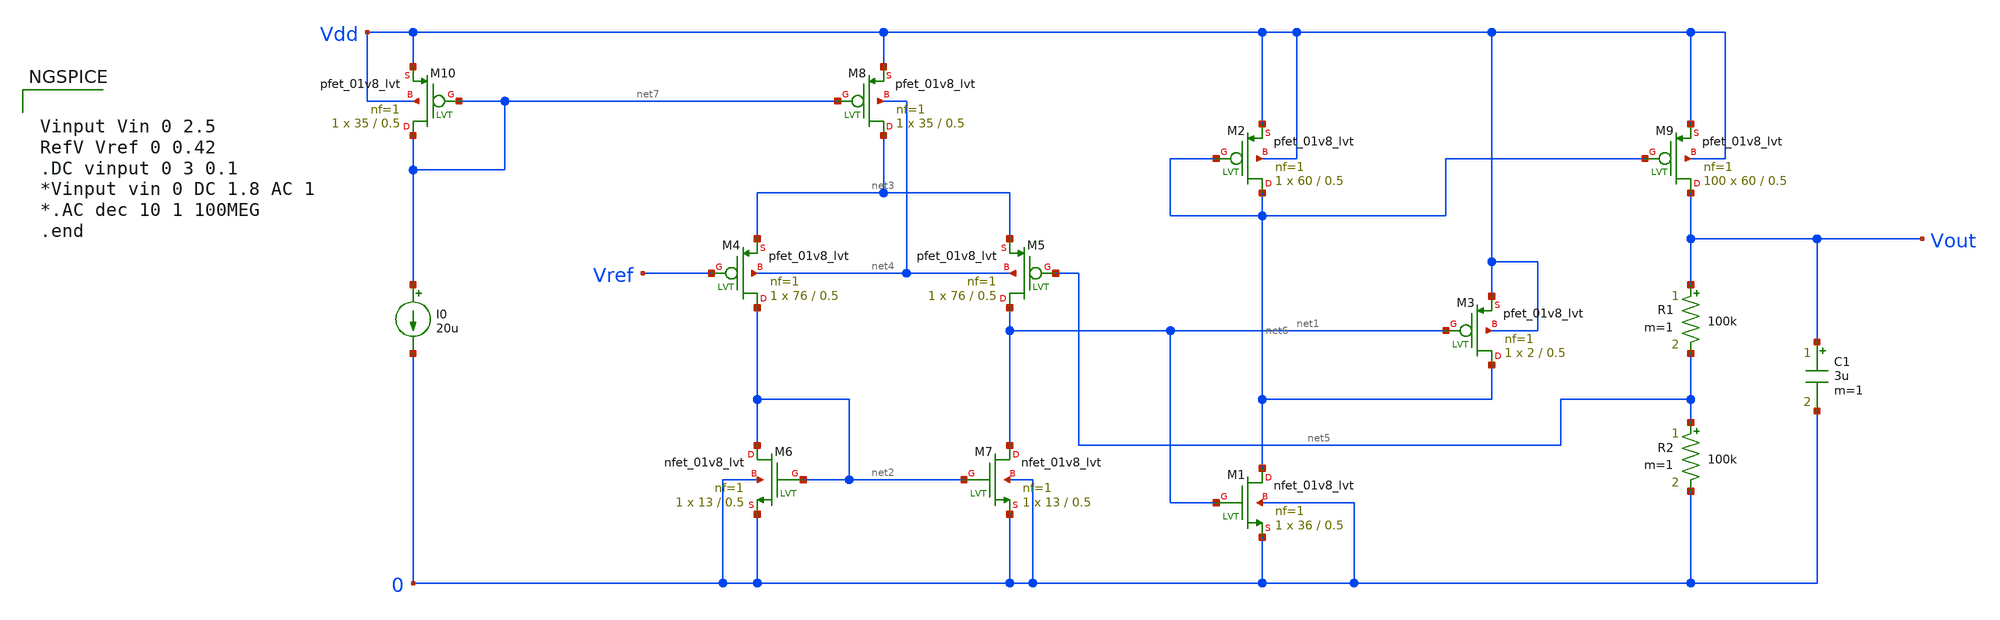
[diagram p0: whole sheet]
** sch_path: LDO/Schematic/Low_PSR_LDO.sch
**.subckt Low_PSR_LDO
XM1 net6 net1 0 0 sky130_fd_pr__nfet_01v8_lvt L=0.5 W=36 nf=1 ad='int((nf+1)/2) * W/nf * 0.29' as='int((nf+2)/2) * W/nf * 0.29'
+ pd='2*int((nf+1)/2) * (W/nf + 0.29)' ps='2*int((nf+2)/2) * (W/nf + 0.29)' nrd='0.29 / W' nrs='0.29 / W'
+ sa=0 sb=0 sd=0 mult=1 m=1
XM2 net6 net6 Vdd Vdd sky130_fd_pr__pfet_01v8_lvt L=0.5 W=60 nf=1 ad='int((nf+1)/2) * W/nf * 0.29' as='int((nf+2)/2) * W/nf * 0.29'
+ pd='2*int((nf+1)/2) * (W/nf + 0.29)' ps='2*int((nf+2)/2) * (W/nf + 0.29)' nrd='0.29 / W' nrs='0.29 / W'
+ sa=0 sb=0 sd=0 mult=1 m=1
XM3 net6 net1 Vdd Vdd sky130_fd_pr__pfet_01v8_lvt L=0.5 W=2 nf=1 ad='int((nf+1)/2) * W/nf * 0.29' as='int((nf+2)/2) * W/nf * 0.29'
+ pd='2*int((nf+1)/2) * (W/nf + 0.29)' ps='2*int((nf+2)/2) * (W/nf + 0.29)' nrd='0.29 / W' nrs='0.29 / W'
+ sa=0 sb=0 sd=0 mult=1 m=1
XM4 net2 Vref net3 net4 sky130_fd_pr__pfet_01v8_lvt L=0.5 W=76 nf=1 ad='int((nf+1)/2) * W/nf * 0.29'
+ as='int((nf+2)/2) * W/nf * 0.29' pd='2*int((nf+1)/2) * (W/nf + 0.29)' ps='2*int((nf+2)/2) * (W/nf + 0.29)'
+ nrd='0.29 / W' nrs='0.29 / W' sa=0 sb=0 sd=0 mult=1 m=1
XM5 net1 net5 net3 net4 sky130_fd_pr__pfet_01v8_lvt L=0.5 W=76 nf=1 ad='int((nf+1)/2) * W/nf * 0.29'
+ as='int((nf+2)/2) * W/nf * 0.29' pd='2*int((nf+1)/2) * (W/nf + 0.29)' ps='2*int((nf+2)/2) * (W/nf + 0.29)'
+ nrd='0.29 / W' nrs='0.29 / W' sa=0 sb=0 sd=0 mult=1 m=1
XM6 net2 net2 0 0 sky130_fd_pr__nfet_01v8_lvt L=0.5 W=13 nf=1 ad='int((nf+1)/2) * W/nf * 0.29' as='int((nf+2)/2) * W/nf * 0.29'
+ pd='2*int((nf+1)/2) * (W/nf + 0.29)' ps='2*int((nf+2)/2) * (W/nf + 0.29)' nrd='0.29 / W' nrs='0.29 / W'
+ sa=0 sb=0 sd=0 mult=1 m=1
XM7 net1 net2 0 0 sky130_fd_pr__nfet_01v8_lvt L=0.5 W=13 nf=1 ad='int((nf+1)/2) * W/nf * 0.29' as='int((nf+2)/2) * W/nf * 0.29'
+ pd='2*int((nf+1)/2) * (W/nf + 0.29)' ps='2*int((nf+2)/2) * (W/nf + 0.29)' nrd='0.29 / W' nrs='0.29 / W'
+ sa=0 sb=0 sd=0 mult=1 m=1
XM8 net3 net7 Vdd net4 sky130_fd_pr__pfet_01v8_lvt L=0.5 W=35 nf=1 ad='int((nf+1)/2) * W/nf * 0.29' as='int((nf+2)/2) * W/nf * 0.29'
+ pd='2*int((nf+1)/2) * (W/nf + 0.29)' ps='2*int((nf+2)/2) * (W/nf + 0.29)' nrd='0.29 / W' nrs='0.29 / W'
+ sa=0 sb=0 sd=0 mult=1 m=1
XM9 Vout net6 Vdd Vdd sky130_fd_pr__pfet_01v8_lvt L=0.5 W=60 nf=1 ad='int((nf+1)/2) * W/nf * 0.29' as='int((nf+2)/2) * W/nf * 0.29'
+ pd='2*int((nf+1)/2) * (W/nf + 0.29)' ps='2*int((nf+2)/2) * (W/nf + 0.29)' nrd='0.29 / W' nrs='0.29 / W'
+ sa=0 sb=0 sd=0 mult=100 m=100
R1 Vout net5 100k m=1
R2 net5 0 100k m=1
C1 Vout 0 3u m=1
XM10 net7 net7 Vdd Vdd sky130_fd_pr__pfet_01v8_lvt L=0.5 W=35 nf=1 ad='int((nf+1)/2) * W/nf * 0.29' as='int((nf+2)/2) * W/nf * 0.29'
+ pd='2*int((nf+1)/2) * (W/nf + 0.29)' ps='2*int((nf+2)/2) * (W/nf + 0.29)' nrd='0.29 / W' nrs='0.29 / W'
+ sa=0 sb=0 sd=0 mult=1 m=1
I0 net7 0 20u
**** begin user architecture code


Vinput Vin 0 2.5
RefV Vref 0 0.42
.DC vinput 0 3 0.1
*Vinput vin 0 DC 1.8 AC 1
*.AC dec 10 1 100MEG
.end



.include $::SKYWATER_MODELS/cells/nfet_01v8/sky130_fd_pr__nfet_01v8__tt.corner.spice
.include $::SKYWATER_MODELS/cells/nfet_01v8_lvt/sky130_fd_pr__nfet_01v8_lvt__tt.corner.spice
.include $::SKYWATER_MODELS/cells/pfet_01v8/sky130_fd_pr__pfet_01v8__tt.corner.spice
.include $::SKYWATER_MODELS/cells/nfet_03v3_nvt/sky130_fd_pr__nfet_03v3_nvt__tt.corner.spice
.include $::SKYWATER_MODELS/cells/nfet_05v0_nvt/sky130_fd_pr__nfet_05v0_nvt__tt.corner.spice
.include $::SKYWATER_MODELS/cells/esd_nfet_01v8/sky130_fd_pr__esd_nfet_01v8__tt.corner.spice
.include $::SKYWATER_MODELS/cells/pfet_01v8_lvt/sky130_fd_pr__pfet_01v8_lvt__tt.corner.spice
.include $::SKYWATER_MODELS/cells/pfet_01v8_hvt/sky130_fd_pr__pfet_01v8_hvt__tt.corner.spice
.include $::SKYWATER_MODELS/cells/esd_pfet_g5v0d10v5/sky130_fd_pr__esd_pfet_g5v0d10v5__tt.corner.spice
.include $::SKYWATER_MODELS/cells/pfet_g5v0d10v5/sky130_fd_pr__pfet_g5v0d10v5__tt.corner.spice
.include $::SKYWATER_MODELS/cells/pfet_g5v0d16v0/sky130_fd_pr__pfet_g5v0d16v0__tt.corner.spice
.include $::SKYWATER_MODELS/cells/nfet_g5v0d10v5/sky130_fd_pr__nfet_g5v0d10v5__tt.corner.spice
.include $::SKYWATER_MODELS/cells/nfet_g5v0d16v0/sky130_fd_pr__nfet_g5v0d16v0__tt_discrete.corner.spice
.include $::SKYWATER_MODELS/cells/esd_nfet_g5v0d10v5/sky130_fd_pr__esd_nfet_g5v0d10v5__tt.corner.spice
.include $::SKYWATER_MODELS/models/corners/tt/nonfet.spice
* Mismatch parameters
.include $::SKYWATER_MODELS/cells/nfet_01v8/sky130_fd_pr__nfet_01v8__mismatch.corner.spice
.include $::SKYWATER_MODELS/cells/pfet_01v8/sky130_fd_pr__pfet_01v8__mismatch.corner.spice
.include $::SKYWATER_MODELS/cells/nfet_01v8_lvt/sky130_fd_pr__nfet_01v8_lvt__mismatch.corner.spice
.include $::SKYWATER_MODELS/cells/pfet_01v8_lvt/sky130_fd_pr__pfet_01v8_lvt__mismatch.corner.spice
.include $::SKYWATER_MODELS/cells/pfet_01v8_hvt/sky130_fd_pr__pfet_01v8_hvt__mismatch.corner.spice
.include $::SKYWATER_MODELS/cells/nfet_g5v0d10v5/sky130_fd_pr__nfet_g5v0d10v5__mismatch.corner.spice
.include $::SKYWATER_MODELS/cells/pfet_g5v0d10v5/sky130_fd_pr__pfet_g5v0d10v5__mismatch.corner.spice
.include $::SKYWATER_MODELS/cells/nfet_05v0_nvt/sky130_fd_pr__nfet_05v0_nvt__mismatch.corner.spice
.include $::SKYWATER_MODELS/cells/nfet_03v3_nvt/sky130_fd_pr__nfet_03v3_nvt__mismatch.corner.spice
* Resistor$::SKYWATER_MODELS/Capacitor
.include $::SKYWATER_MODELS/models/r+c/res_typical__cap_typical.spice
.include $::SKYWATER_MODELS/models/r+c/res_typical__cap_typical__lin.spice
* Special cells
.include $::SKYWATER_MODELS/models/corners/tt/specialized_cells.spice
* All models
.include $::SKYWATER_MODELS/models/all.spice
* Corner
.include $::SKYWATER_MODELS/models/corners/tt/rf.spice

**** end user architecture code
**.ends
.end
